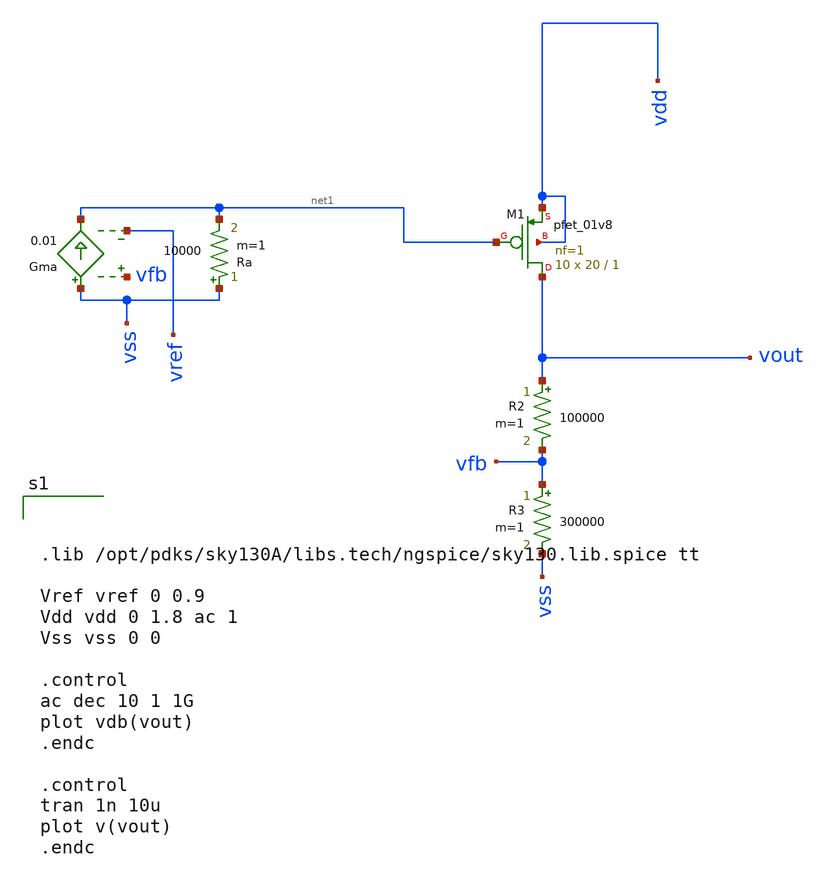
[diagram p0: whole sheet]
** sch_path: test-python/result_comp/xschem/ldo_pt_tb.sch
**.subckt ldo_pt_tb
R2 vout vfb 100000 m=1
R3 vfb vss 300000 m=1
Gma vss net1 vfb vref 0.01
Ra vss net1 10000 m=1
XM1 vout net1 vdd vdd sky130_fd_pr__pfet_01v8 L=1 W=20 nf=1 ad='int((nf+1)/2) * W/nf * 0.29' as='int((nf+2)/2) * W/nf * 0.29'
+ pd='2*int((nf+1)/2) * (W/nf + 0.29)' ps='2*int((nf+2)/2) * (W/nf + 0.29)' nrd='0.29 / W' nrs='0.29 / W'
+ sa=0 sb=0 sd=0 mult=10 m=10
**** begin user architecture code



.lib /opt/pdks/sky130A/libs.tech/ngspice/sky130.lib.spice tt

Vref vref 0 0.9
Vdd vdd 0 1.8 ac 1
Vss vss 0 0

.control
ac dec 10 1 1G
plot vdb(vout)
.endc

.control
tran 1n 10u
plot v(vout)
.endc



**** end user architecture code
**.ends
.end
